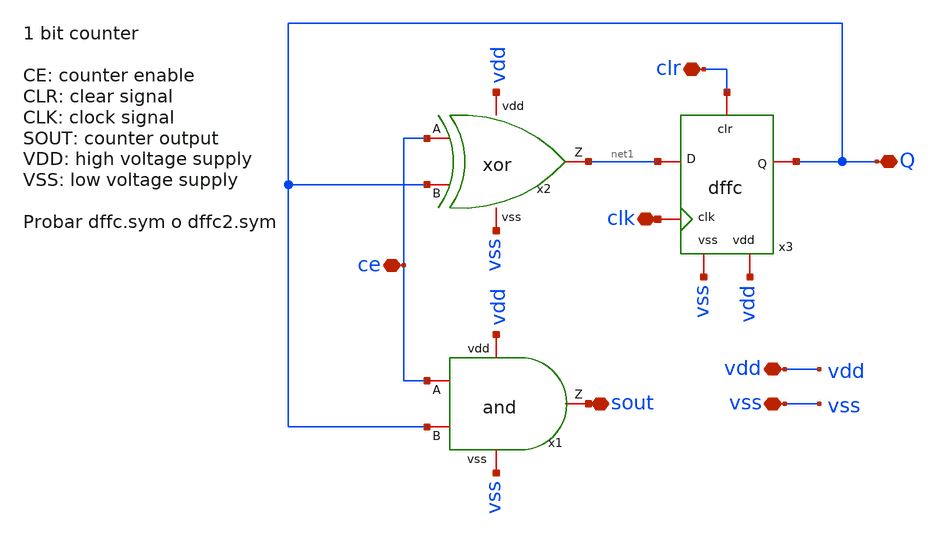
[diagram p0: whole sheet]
** sch_path: designs/sch/1BitCounter.sch
**.subckt 1BitCounter clk sout ce clr vdd vss Q
*.iopin clk
*.iopin sout
*.iopin ce
*.iopin clr
*.iopin vdd
*.iopin vss
*.iopin Q
x1 vdd ce sout Q vss and
x2 vdd net1 ce Q vss xor
x3 Q net1 clk clr vss vdd dffc
**.ends
.end
